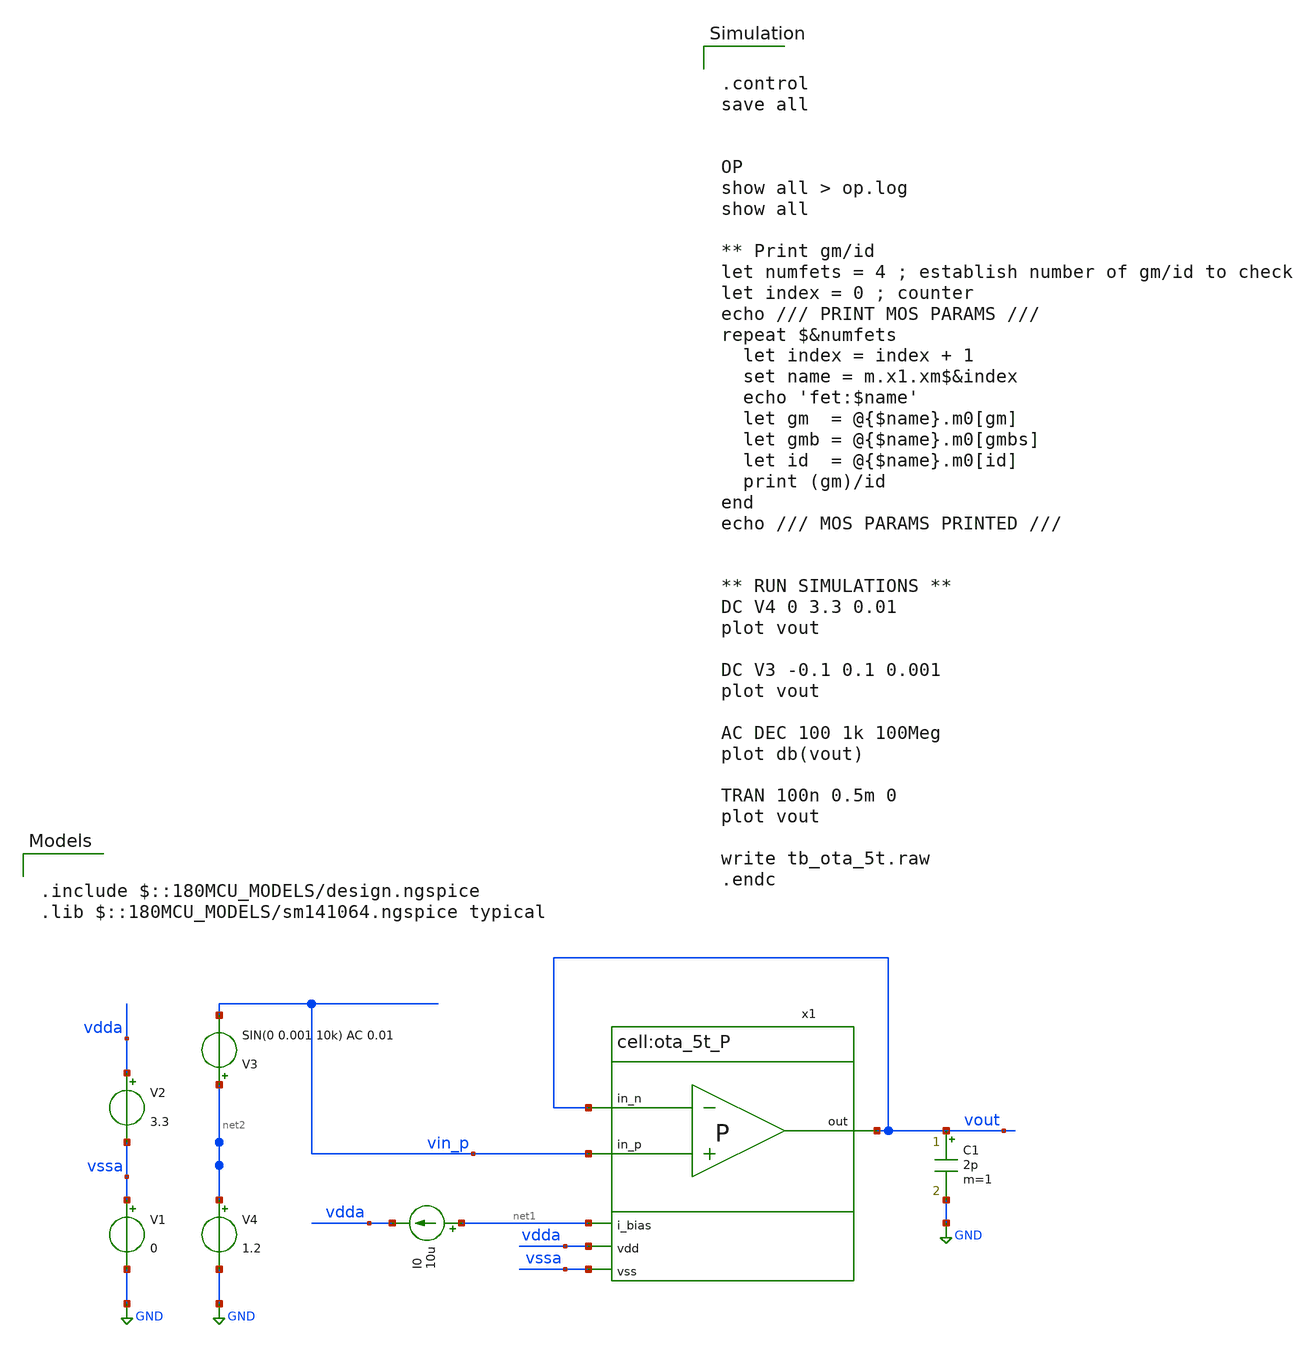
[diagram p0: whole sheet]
** sch_path: designs/switch_matrix_gf180mcu_9t5v0-main/designs/libs/tb_analog/tb_ota_5t_dc/tb_ota_5t_p_dc.sch
**.subckt tb_ota_5t_p_dc
V1 vssa GND 0
V2 vdda vssa 3.3
I0 net1 vdda 10u
V3 net2 vin_p SIN(0 0.001 10k) AC 0.01
V4 net2 GND 1.2
C1 vout GND 2p m=1
x1 vdda vout vin_p vout net1 vssa ota_5t_P
**** begin user architecture code


.control
save all


OP
show all > op.log
show all

** Print gm/id
let numfets = 4 ; establish number of gm/id to check
let index = 0 ; counter
echo /// PRINT MOS PARAMS ///
repeat $&numfets
  let index = index + 1
  set name = m.x1.xm$&index
  echo 'fet:$name'
  let gm  = @{$name}.m0[gm]
  let gmb = @{$name}.m0[gmbs]
  let id  = @{$name}.m0[id]
  print (gm)/id
end
echo /// MOS PARAMS PRINTED ///


** RUN SIMULATIONS **
DC V4 0 3.3 0.01
plot vout

DC V3 -0.1 0.1 0.001
plot vout

AC DEC 100 1k 100Meg
plot db(vout)

TRAN 100n 0.5m 0
plot vout

write tb_ota_5t.raw
.endc



.include $::180MCU_MODELS/design.ngspice
.lib $::180MCU_MODELS/sm141064.ngspice typical

**** end user architecture code
**.ends
.GLOBAL GND
.end
